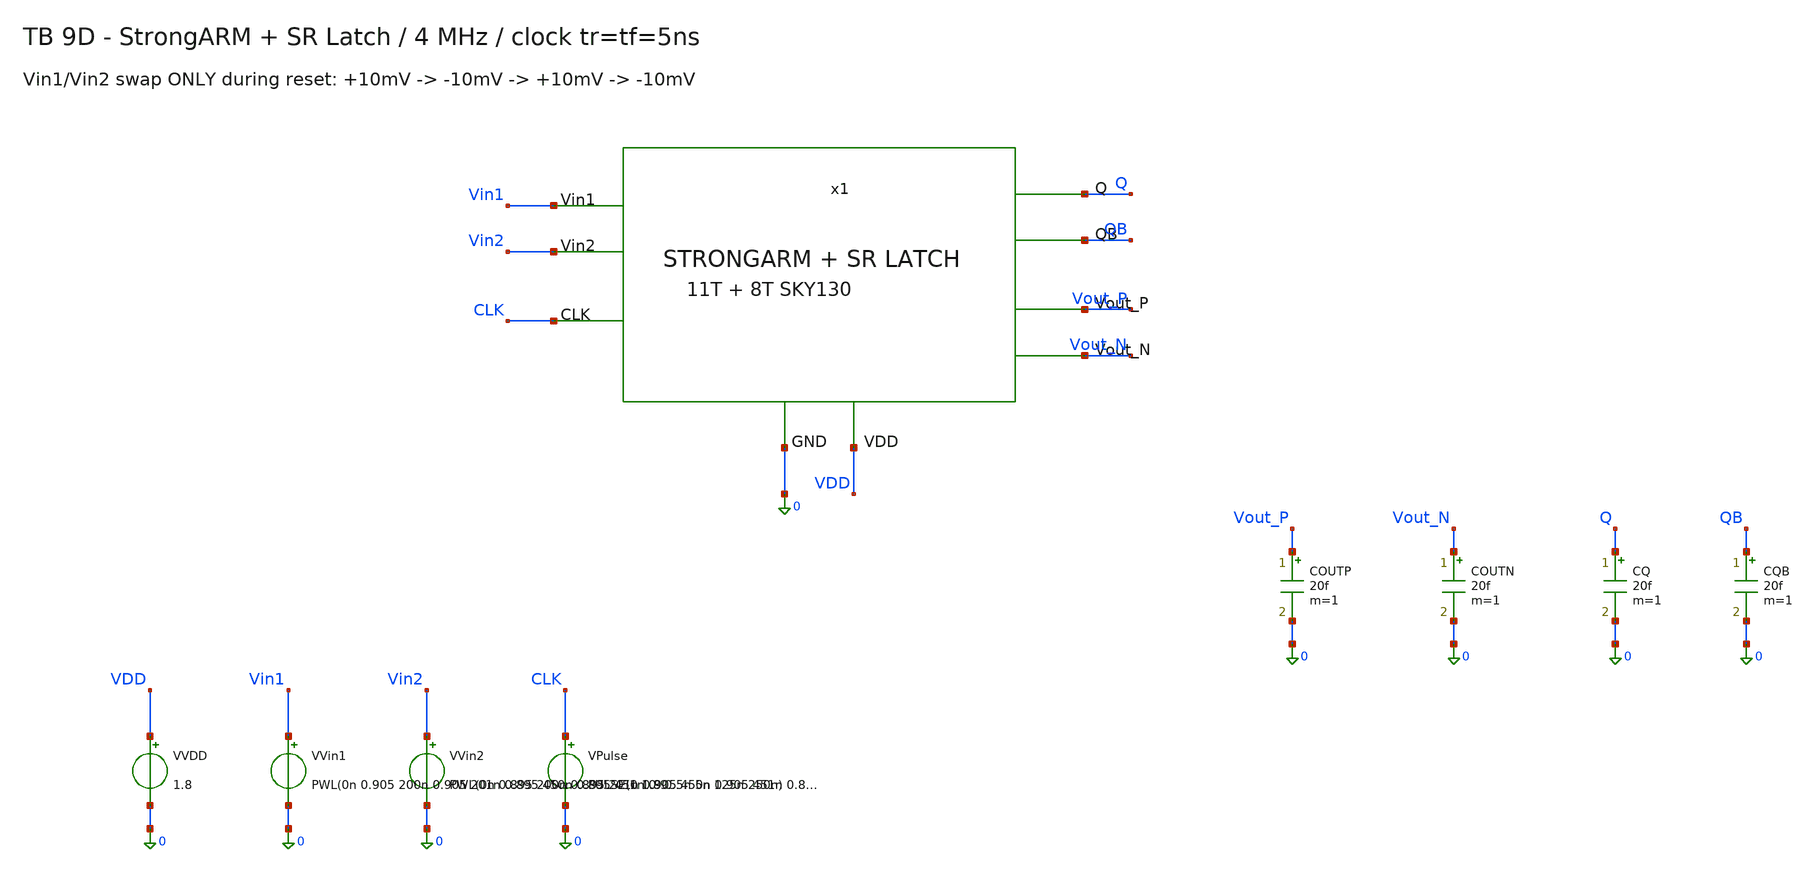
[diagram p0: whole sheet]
** sch_path: blocks/03_StrongARM/sim/tb_StrongARM_Latch.sch
**.subckt tb_StrongARM_Latch
x1 Vin1 Vin2 CLK VDD 0 Q QB Vout_P Vout_N StrongARM_Latch
VVDD VDD 0 1.8
VVin1 Vin1 0 PWL(0n 0.905 200n 0.905 201n 0.895 450n 0.895 451n 0.905 700n 0.905 701n 0.895 1000n
+ 0.895)
VVin2 Vin2 0 PWL(0n 0.895 200n 0.895 201n 0.905 450n 0.905 451n 0.895 700n 0.895 701n 0.905 1000n
+ 0.905)
VPulse CLK 0 PULSE(0 1.8 0 5n 5n 125n 250n)
COUTP Vout_P 0 20f m=1
COUTN Vout_N 0 20f m=1
CQ Q 0 20f m=1
CQB QB 0 20f m=1
**** begin user architecture code

.lib /foss/pdks/sky130A/libs.tech/combined/sky130.lib.spice tt
.option scale=1e-6
.tran 0.02n 1u 0 0.02n
.meas tran eval1_q FIND v(q) AT=40n
.meas tran eval1_qb FIND v(qb) AT=40n
.meas tran eval1_vout_p FIND v(vout_p) AT=40n
.meas tran eval1_vout_n FIND v(vout_n) AT=40n
.meas tran hold1_q FIND v(q) AT=180n
.meas tran hold1_qb FIND v(qb) AT=180n
.meas tran hold1_vout_p FIND v(vout_p) AT=180n
.meas tran hold1_vout_n FIND v(vout_n) AT=180n
.meas tran input_hold1_q FIND v(q) AT=225n
.meas tran input_hold1_qb FIND v(qb) AT=225n
.meas tran input_hold1_vout_p FIND v(vout_p) AT=225n
.meas tran input_hold1_vout_n FIND v(vout_n) AT=225n
.meas tran eval2_q FIND v(q) AT=290n
.meas tran eval2_qb FIND v(qb) AT=290n
.meas tran eval2_vout_p FIND v(vout_p) AT=290n
.meas tran eval2_vout_n FIND v(vout_n) AT=290n
.meas tran hold2_q FIND v(q) AT=430n
.meas tran hold2_qb FIND v(qb) AT=430n
.meas tran hold2_vout_p FIND v(vout_p) AT=430n
.meas tran hold2_vout_n FIND v(vout_n) AT=430n
.meas tran input_hold2_q FIND v(q) AT=475n
.meas tran input_hold2_qb FIND v(qb) AT=475n
.meas tran input_hold2_vout_p FIND v(vout_p) AT=475n
.meas tran input_hold2_vout_n FIND v(vout_n) AT=475n
.meas tran eval3_q FIND v(q) AT=540n
.meas tran eval3_qb FIND v(qb) AT=540n
.meas tran eval3_vout_p FIND v(vout_p) AT=540n
.meas tran eval3_vout_n FIND v(vout_n) AT=540n
.meas tran hold3_q FIND v(q) AT=680n
.meas tran hold3_qb FIND v(qb) AT=680n
.meas tran hold3_vout_p FIND v(vout_p) AT=680n
.meas tran hold3_vout_n FIND v(vout_n) AT=680n
.meas tran input_hold3_q FIND v(q) AT=725n
.meas tran input_hold3_qb FIND v(qb) AT=725n
.meas tran input_hold3_vout_p FIND v(vout_p) AT=725n
.meas tran input_hold3_vout_n FIND v(vout_n) AT=725n
.meas tran eval4_q FIND v(q) AT=790n
.meas tran eval4_qb FIND v(qb) AT=790n
.meas tran eval4_vout_p FIND v(vout_p) AT=790n
.meas tran eval4_vout_n FIND v(vout_n) AT=790n
.meas tran hold4_q FIND v(q) AT=930n
.meas tran hold4_qb FIND v(qb) AT=930n
.meas tran hold4_vout_p FIND v(vout_p) AT=930n
.meas tran hold4_vout_n FIND v(vout_n) AT=930n
.meas tran iavg AVG i(VVDD) FROM=250n TO=1000n
.meas tran t_c2 TRIG v(CLK) VAL=0.9 RISE=2 TARG v(Q) VAL=0.9 FALL=1 TD=240n
.meas tran t_c3 TRIG v(CLK) VAL=0.9 RISE=3 TARG v(Q) VAL=0.9 RISE=1 TD=490n
.meas tran t_c4 TRIG v(CLK) VAL=0.9 RISE=4 TARG v(Q) VAL=0.9 FALL=1 TD=740n
.save v(CLK) v(Vin1) v(Vin2) v(Vout_P) v(Vout_N) v(Q) v(QB) v(VDD) i(VVDD)

**** end user architecture code
**.ends

* expanding   symbol:  blocks/03_StrongARM/xschem/StrongARM_Latch.sym # of pins=9
** sym_path: blocks/03_StrongARM/xschem/StrongARM_Latch.sym
** sch_path: blocks/03_StrongARM/xschem/StrongARM_Latch.sch
.subckt StrongARM_Latch Vin1 Vin2 CLK VDD GND Q QB Vout_P Vout_N
*.ipin Vin1
*.ipin Vin2
*.ipin CLK
*.iopin VDD
*.iopin GND
*.opin Q
*.opin QB
*.opin Vout_P
*.opin Vout_N
xSA VDD CLK Vout_P Vout_N Vin1 Vin2 GND StrongARM
xSR Vout_P Vout_N Q QB GND VDD SR_Latch
.ends


* expanding   symbol:  blocks/03_StrongARM/xschem/StrongARM.sym # of pins=7
** sym_path: blocks/03_StrongARM/xschem/StrongARM.sym
** sch_path: blocks/03_StrongARM/xschem/StrongARM.sch
.subckt StrongARM VDD CLK Vout_P Vout_N Vin1 Vin2 GND
*.iopin VDD
*.iopin GND
*.ipin Vin1
*.ipin Vin2
*.ipin CLK
*.opin Vout_P
*.opin Vout_N
XS1 P CLK VDD VDD sky130_fd_pr__pfet_01v8 L=0.15 W=1.5 nf=1 ad='int((1 + 1)/2) * 1.5 / 1 * 0.29' as='int((1 + 2)/2) * 1.5 / 1 * 0.29'
+ pd='2*int((1 + 1)/2) * (1.5 / 1 + 0.29)' ps='2*int((1 + 2)/2) * (1.5 / 1 + 0.29)' nrd='0.29 / 1.5 ' nrs='0.29 / 1.5 '
+ sa=0 sb=0 sd=0 mult=1 m=1
XS3 Vout_P CLK VDD VDD sky130_fd_pr__pfet_01v8 L=0.15 W=1.5 nf=1 ad='int((1 + 1)/2) * 1.5 / 1 * 0.29'
+ as='int((1 + 2)/2) * 1.5 / 1 * 0.29' pd='2*int((1 + 1)/2) * (1.5 / 1 + 0.29)' ps='2*int((1 + 2)/2) * (1.5 / 1 + 0.29)'
+ nrd='0.29 / 1.5 ' nrs='0.29 / 1.5 ' sa=0 sb=0 sd=0 mult=1 m=1
XM5 Vout_P Vout_N VDD VDD sky130_fd_pr__pfet_01v8 L=0.3 W=5 nf=1 ad='int((1 + 1)/2) * 5 / 1 * 0.29' as='int((1 + 2)/2) * 5 / 1 * 0.29'
+ pd='2*int((1 + 1)/2) * (5 / 1 + 0.29)' ps='2*int((1 + 2)/2) * (5 / 1 + 0.29)' nrd='0.29 / 5 ' nrs='0.29 / 5 '
+ sa=0 sb=0 sd=0 mult=1 m=1
XM6 Vout_N Vout_P VDD VDD sky130_fd_pr__pfet_01v8 L=0.3 W=5 nf=1 ad='int((1 + 1)/2) * 5 / 1 * 0.29' as='int((1 + 2)/2) * 5 / 1 * 0.29'
+ pd='2*int((1 + 1)/2) * (5 / 1 + 0.29)' ps='2*int((1 + 2)/2) * (5 / 1 + 0.29)' nrd='0.29 / 5 ' nrs='0.29 / 5 '
+ sa=0 sb=0 sd=0 mult=1 m=1
XS4 Vout_N CLK VDD VDD sky130_fd_pr__pfet_01v8 L=0.15 W=1.5 nf=1 ad='int((1 + 1)/2) * 1.5 / 1 * 0.29'
+ as='int((1 + 2)/2) * 1.5 / 1 * 0.29' pd='2*int((1 + 1)/2) * (1.5 / 1 + 0.29)' ps='2*int((1 + 2)/2) * (1.5 / 1 + 0.29)'
+ nrd='0.29 / 1.5 ' nrs='0.29 / 1.5 ' sa=0 sb=0 sd=0 mult=1 m=1
XS2 Q CLK VDD VDD sky130_fd_pr__pfet_01v8 L=0.15 W=1.5 nf=1 ad='int((1 + 1)/2) * 1.5 / 1 * 0.29' as='int((1 + 2)/2) * 1.5 / 1 * 0.29'
+ pd='2*int((1 + 1)/2) * (1.5 / 1 + 0.29)' ps='2*int((1 + 2)/2) * (1.5 / 1 + 0.29)' nrd='0.29 / 1.5 ' nrs='0.29 / 1.5 '
+ sa=0 sb=0 sd=0 mult=1 m=1
XM3 Vout_P Vout_N P GND sky130_fd_pr__nfet_01v8 L=0.3 W=2 nf=1 ad='int((1 + 1)/2) * 2 / 1 * 0.29' as='int((1 + 2)/2) * 2 / 1 * 0.29'
+ pd='2*int((1 + 1)/2) * (2 / 1 + 0.29)' ps='2*int((1 + 2)/2) * (2 / 1 + 0.29)' nrd='0.29 / 2 ' nrs='0.29 / 2 '
+ sa=0 sb=0 sd=0 mult=1 m=1
XM4 Vout_N Vout_P Q GND sky130_fd_pr__nfet_01v8 L=0.3 W=2 nf=1 ad='int((1 + 1)/2) * 2 / 1 * 0.29' as='int((1 + 2)/2) * 2 / 1 * 0.29'
+ pd='2*int((1 + 1)/2) * (2 / 1 + 0.29)' ps='2*int((1 + 2)/2) * (2 / 1 + 0.29)' nrd='0.29 / 2 ' nrs='0.29 / 2 '
+ sa=0 sb=0 sd=0 mult=1 m=1
XM1 P Vin1 TAIL GND sky130_fd_pr__nfet_01v8 L=0.5 W=10 nf=1 ad='int((1 + 1)/2) * 10 / 1 * 0.29' as='int((1 + 2)/2) * 10 / 1 * 0.29'
+ pd='2*int((1 + 1)/2) * (10 / 1 + 0.29)' ps='2*int((1 + 2)/2) * (10 / 1 + 0.29)' nrd='0.29 / 10 ' nrs='0.29 / 10 '
+ sa=0 sb=0 sd=0 mult=1 m=1
XM2 Q Vin2 TAIL GND sky130_fd_pr__nfet_01v8 L=0.5 W=10 nf=1 ad='int((1 + 1)/2) * 10 / 1 * 0.29' as='int((1 + 2)/2) * 10 / 1 * 0.29'
+ pd='2*int((1 + 1)/2) * (10 / 1 + 0.29)' ps='2*int((1 + 2)/2) * (10 / 1 + 0.29)' nrd='0.29 / 10 ' nrs='0.29 / 10 '
+ sa=0 sb=0 sd=0 mult=1 m=1
XM7 TAIL CLK GND GND sky130_fd_pr__nfet_01v8 L=0.3 W=1 nf=1 ad='int((1 + 1)/2) * 1 / 1 * 0.29' as='int((1 + 2)/2) * 1 / 1 * 0.29'
+ pd='2*int((1 + 1)/2) * (1 / 1 + 0.29)' ps='2*int((1 + 2)/2) * (1 / 1 + 0.29)' nrd='0.29 / 1 ' nrs='0.29 / 1 '
+ sa=0 sb=0 sd=0 mult=1 m=1
.ends


* expanding   symbol:  blocks/03_StrongARM/xschem/SR_Latch.sym # of pins=6
** sym_path: blocks/03_StrongARM/xschem/SR_Latch.sym
** sch_path: blocks/03_StrongARM/xschem/SR_Latch.sch
.subckt SR_Latch SN RN Q QB GND VCC
*.ipin SN
*.ipin RN
*.opin Q
*.opin QB
*.iopin VCC
*.iopin GND
x1 SN QB Q GND VCC NAND2
x2 RN Q QB GND VCC NAND2
.ends


* expanding   symbol:  blocks/03_StrongARM/xschem/NAND2.sym # of pins=5
** sym_path: blocks/03_StrongARM/xschem/NAND2.sym
** sch_path: blocks/03_StrongARM/xschem/NAND2.sch
.subckt NAND2 A B Y GND VCC
*.iopin VCC
*.iopin GND
*.ipin A
*.ipin B
*.opin Y
XM1 Y A VCC VCC sky130_fd_pr__pfet_01v8 L=0.15 W=2 nf=1 ad='int((1 + 1)/2) * 2 / 1 * 0.29' as='int((1 + 2)/2) * 2 / 1 * 0.29'
+ pd='2*int((1 + 1)/2) * (2 / 1 + 0.29)' ps='2*int((1 + 2)/2) * (2 / 1 + 0.29)' nrd='0.29 / 2 ' nrs='0.29 / 2 '
+ sa=0 sb=0 sd=0 mult=1 m=1
XM2 Y B VCC VCC sky130_fd_pr__pfet_01v8 L=0.15 W=2 nf=1 ad='int((1 + 1)/2) * 2 / 1 * 0.29' as='int((1 + 2)/2) * 2 / 1 * 0.29'
+ pd='2*int((1 + 1)/2) * (2 / 1 + 0.29)' ps='2*int((1 + 2)/2) * (2 / 1 + 0.29)' nrd='0.29 / 2 ' nrs='0.29 / 2 '
+ sa=0 sb=0 sd=0 mult=1 m=1
XM3 Y A net1 GND sky130_fd_pr__nfet_01v8 L=0.15 W=2 nf=1 ad='int((1 + 1)/2) * 2 / 1 * 0.29' as='int((1 + 2)/2) * 2 / 1 * 0.29'
+ pd='2*int((1 + 1)/2) * (2 / 1 + 0.29)' ps='2*int((1 + 2)/2) * (2 / 1 + 0.29)' nrd='0.29 / 2 ' nrs='0.29 / 2 '
+ sa=0 sb=0 sd=0 mult=1 m=1
XM4 net1 B GND GND sky130_fd_pr__nfet_01v8 L=0.15 W=2 nf=1 ad='int((1 + 1)/2) * 2 / 1 * 0.29' as='int((1 + 2)/2) * 2 / 1 * 0.29'
+ pd='2*int((1 + 1)/2) * (2 / 1 + 0.29)' ps='2*int((1 + 2)/2) * (2 / 1 + 0.29)' nrd='0.29 / 2 ' nrs='0.29 / 2 '
+ sa=0 sb=0 sd=0 mult=1 m=1
.ends

.end
